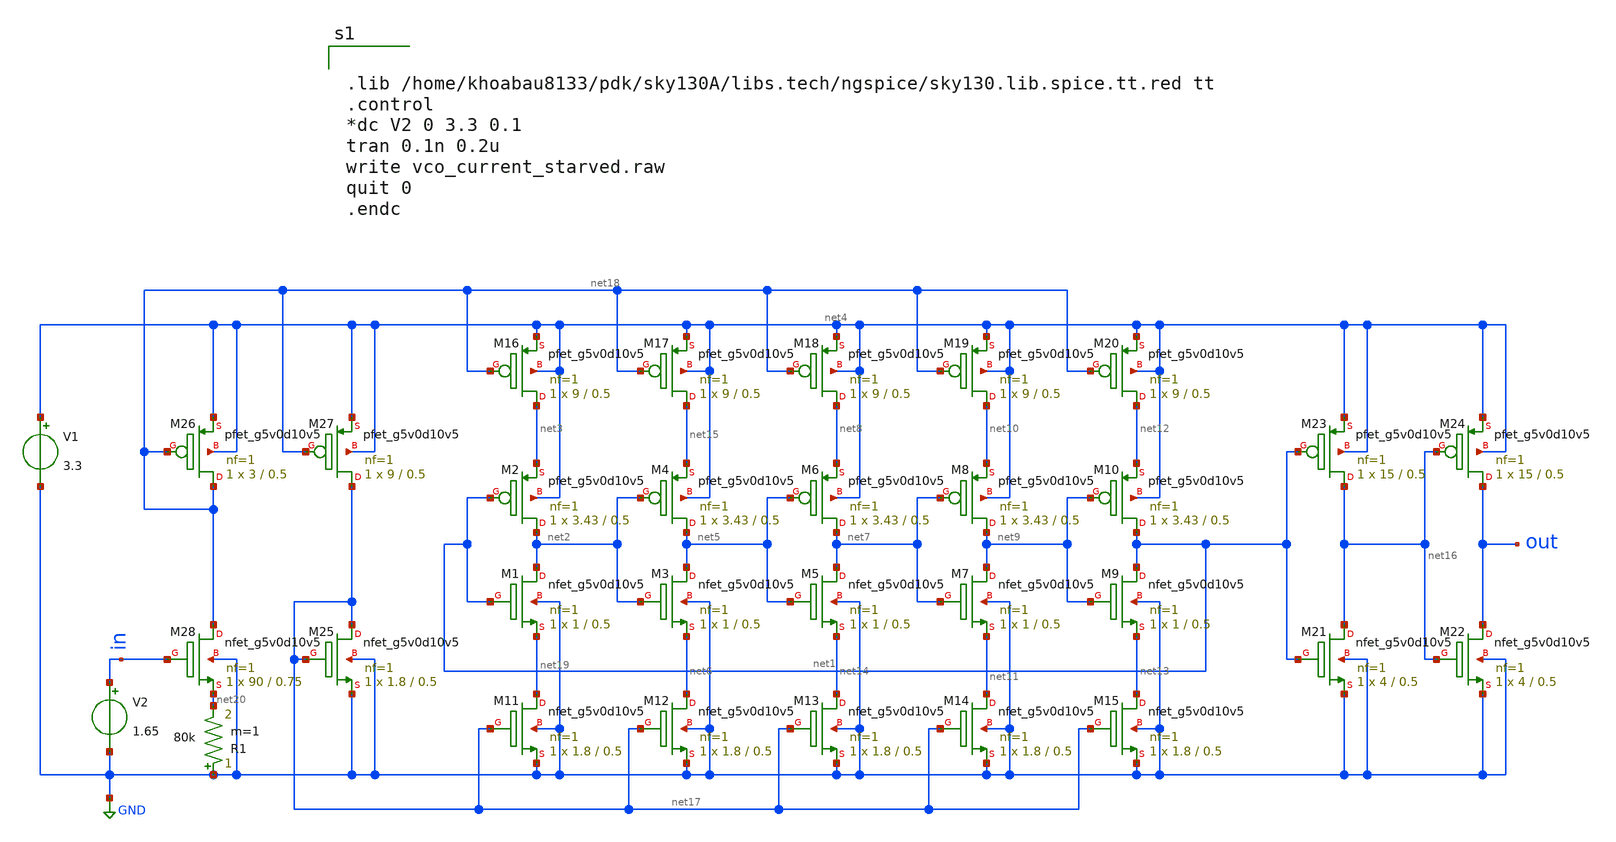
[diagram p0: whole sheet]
** sch_path: Voltage-controlled Oscillator/test_VCO_v3.sch
**.subckt test_VCO_v3
V1 net4 GND 3.3
V2 in GND 1.65
R1 GND net20 80k m=1
XM1 net2 net1 net19 GND sky130_fd_pr__nfet_g5v0d10v5 L=0.5 W=1 nf=1 ad='int((nf+1)/2) * W/nf * 0.29'
+ as='int((nf+2)/2) * W/nf * 0.29' pd='2*int((nf+1)/2) * (W/nf + 0.29)' ps='2*int((nf+2)/2) * (W/nf + 0.29)'
+ nrd='0.29 / W' nrs='0.29 / W' sa=0 sb=0 sd=0 mult=1 m=1
XM2 net2 net1 net3 net4 sky130_fd_pr__pfet_g5v0d10v5 L=0.5 W=3.43 nf=1 ad='int((nf+1)/2) * W/nf * 0.29'
+ as='int((nf+2)/2) * W/nf * 0.29' pd='2*int((nf+1)/2) * (W/nf + 0.29)' ps='2*int((nf+2)/2) * (W/nf + 0.29)'
+ nrd='0.29 / W' nrs='0.29 / W' sa=0 sb=0 sd=0 mult=1 m=1
XM3 net5 net2 net6 GND sky130_fd_pr__nfet_g5v0d10v5 L=0.5 W=1 nf=1 ad='int((nf+1)/2) * W/nf * 0.29' as='int((nf+2)/2) * W/nf * 0.29'
+ pd='2*int((nf+1)/2) * (W/nf + 0.29)' ps='2*int((nf+2)/2) * (W/nf + 0.29)' nrd='0.29 / W' nrs='0.29 / W'
+ sa=0 sb=0 sd=0 mult=1 m=1
XM4 net5 net2 net15 net4 sky130_fd_pr__pfet_g5v0d10v5 L=0.5 W=3.43 nf=1 ad='int((nf+1)/2) * W/nf * 0.29'
+ as='int((nf+2)/2) * W/nf * 0.29' pd='2*int((nf+1)/2) * (W/nf + 0.29)' ps='2*int((nf+2)/2) * (W/nf + 0.29)'
+ nrd='0.29 / W' nrs='0.29 / W' sa=0 sb=0 sd=0 mult=1 m=1
XM5 net7 net5 net14 GND sky130_fd_pr__nfet_g5v0d10v5 L=0.5 W=1 nf=1 ad='int((nf+1)/2) * W/nf * 0.29'
+ as='int((nf+2)/2) * W/nf * 0.29' pd='2*int((nf+1)/2) * (W/nf + 0.29)' ps='2*int((nf+2)/2) * (W/nf + 0.29)'
+ nrd='0.29 / W' nrs='0.29 / W' sa=0 sb=0 sd=0 mult=1 m=1
XM6 net7 net5 net8 net4 sky130_fd_pr__pfet_g5v0d10v5 L=0.5 W=3.43 nf=1 ad='int((nf+1)/2) * W/nf * 0.29'
+ as='int((nf+2)/2) * W/nf * 0.29' pd='2*int((nf+1)/2) * (W/nf + 0.29)' ps='2*int((nf+2)/2) * (W/nf + 0.29)'
+ nrd='0.29 / W' nrs='0.29 / W' sa=0 sb=0 sd=0 mult=1 m=1
XM7 net9 net7 net11 GND sky130_fd_pr__nfet_g5v0d10v5 L=0.5 W=1 nf=1 ad='int((nf+1)/2) * W/nf * 0.29'
+ as='int((nf+2)/2) * W/nf * 0.29' pd='2*int((nf+1)/2) * (W/nf + 0.29)' ps='2*int((nf+2)/2) * (W/nf + 0.29)'
+ nrd='0.29 / W' nrs='0.29 / W' sa=0 sb=0 sd=0 mult=1 m=1
XM8 net9 net7 net10 net4 sky130_fd_pr__pfet_g5v0d10v5 L=0.5 W=3.43 nf=1 ad='int((nf+1)/2) * W/nf * 0.29'
+ as='int((nf+2)/2) * W/nf * 0.29' pd='2*int((nf+1)/2) * (W/nf + 0.29)' ps='2*int((nf+2)/2) * (W/nf + 0.29)'
+ nrd='0.29 / W' nrs='0.29 / W' sa=0 sb=0 sd=0 mult=1 m=1
XM9 net1 net9 net13 GND sky130_fd_pr__nfet_g5v0d10v5 L=0.5 W=1 nf=1 ad='int((nf+1)/2) * W/nf * 0.29'
+ as='int((nf+2)/2) * W/nf * 0.29' pd='2*int((nf+1)/2) * (W/nf + 0.29)' ps='2*int((nf+2)/2) * (W/nf + 0.29)'
+ nrd='0.29 / W' nrs='0.29 / W' sa=0 sb=0 sd=0 mult=1 m=1
XM10 net1 net9 net12 net4 sky130_fd_pr__pfet_g5v0d10v5 L=0.5 W=3.43 nf=1 ad='int((nf+1)/2) * W/nf * 0.29'
+ as='int((nf+2)/2) * W/nf * 0.29' pd='2*int((nf+1)/2) * (W/nf + 0.29)' ps='2*int((nf+2)/2) * (W/nf + 0.29)'
+ nrd='0.29 / W' nrs='0.29 / W' sa=0 sb=0 sd=0 mult=1 m=1
XM11 net19 net17 GND GND sky130_fd_pr__nfet_g5v0d10v5 L=0.5 W=1.8 nf=1 ad='int((nf+1)/2) * W/nf * 0.29'
+ as='int((nf+2)/2) * W/nf * 0.29' pd='2*int((nf+1)/2) * (W/nf + 0.29)' ps='2*int((nf+2)/2) * (W/nf + 0.29)'
+ nrd='0.29 / W' nrs='0.29 / W' sa=0 sb=0 sd=0 mult=1 m=1
XM12 net6 net17 GND GND sky130_fd_pr__nfet_g5v0d10v5 L=0.5 W=1.8 nf=1 ad='int((nf+1)/2) * W/nf * 0.29'
+ as='int((nf+2)/2) * W/nf * 0.29' pd='2*int((nf+1)/2) * (W/nf + 0.29)' ps='2*int((nf+2)/2) * (W/nf + 0.29)'
+ nrd='0.29 / W' nrs='0.29 / W' sa=0 sb=0 sd=0 mult=1 m=1
XM13 net14 net17 GND GND sky130_fd_pr__nfet_g5v0d10v5 L=0.5 W=1.8 nf=1 ad='int((nf+1)/2) * W/nf * 0.29'
+ as='int((nf+2)/2) * W/nf * 0.29' pd='2*int((nf+1)/2) * (W/nf + 0.29)' ps='2*int((nf+2)/2) * (W/nf + 0.29)'
+ nrd='0.29 / W' nrs='0.29 / W' sa=0 sb=0 sd=0 mult=1 m=1
XM14 net11 net17 GND GND sky130_fd_pr__nfet_g5v0d10v5 L=0.5 W=1.8 nf=1 ad='int((nf+1)/2) * W/nf * 0.29'
+ as='int((nf+2)/2) * W/nf * 0.29' pd='2*int((nf+1)/2) * (W/nf + 0.29)' ps='2*int((nf+2)/2) * (W/nf + 0.29)'
+ nrd='0.29 / W' nrs='0.29 / W' sa=0 sb=0 sd=0 mult=1 m=1
XM15 net13 net17 GND GND sky130_fd_pr__nfet_g5v0d10v5 L=0.5 W=1.8 nf=1 ad='int((nf+1)/2) * W/nf * 0.29'
+ as='int((nf+2)/2) * W/nf * 0.29' pd='2*int((nf+1)/2) * (W/nf + 0.29)' ps='2*int((nf+2)/2) * (W/nf + 0.29)'
+ nrd='0.29 / W' nrs='0.29 / W' sa=0 sb=0 sd=0 mult=1 m=1
XM16 net3 net18 net4 net4 sky130_fd_pr__pfet_g5v0d10v5 L=0.5 W=9 nf=1 ad='int((nf+1)/2) * W/nf * 0.29'
+ as='int((nf+2)/2) * W/nf * 0.29' pd='2*int((nf+1)/2) * (W/nf + 0.29)' ps='2*int((nf+2)/2) * (W/nf + 0.29)'
+ nrd='0.29 / W' nrs='0.29 / W' sa=0 sb=0 sd=0 mult=1 m=1
XM17 net15 net18 net4 net4 sky130_fd_pr__pfet_g5v0d10v5 L=0.5 W=9 nf=1 ad='int((nf+1)/2) * W/nf * 0.29'
+ as='int((nf+2)/2) * W/nf * 0.29' pd='2*int((nf+1)/2) * (W/nf + 0.29)' ps='2*int((nf+2)/2) * (W/nf + 0.29)'
+ nrd='0.29 / W' nrs='0.29 / W' sa=0 sb=0 sd=0 mult=1 m=1
XM18 net8 net18 net4 net4 sky130_fd_pr__pfet_g5v0d10v5 L=0.5 W=9 nf=1 ad='int((nf+1)/2) * W/nf * 0.29'
+ as='int((nf+2)/2) * W/nf * 0.29' pd='2*int((nf+1)/2) * (W/nf + 0.29)' ps='2*int((nf+2)/2) * (W/nf + 0.29)'
+ nrd='0.29 / W' nrs='0.29 / W' sa=0 sb=0 sd=0 mult=1 m=1
XM19 net10 net18 net4 net4 sky130_fd_pr__pfet_g5v0d10v5 L=0.5 W=9 nf=1 ad='int((nf+1)/2) * W/nf * 0.29'
+ as='int((nf+2)/2) * W/nf * 0.29' pd='2*int((nf+1)/2) * (W/nf + 0.29)' ps='2*int((nf+2)/2) * (W/nf + 0.29)'
+ nrd='0.29 / W' nrs='0.29 / W' sa=0 sb=0 sd=0 mult=1 m=1
XM20 net12 net18 net4 net4 sky130_fd_pr__pfet_g5v0d10v5 L=0.5 W=9 nf=1 ad='int((nf+1)/2) * W/nf * 0.29'
+ as='int((nf+2)/2) * W/nf * 0.29' pd='2*int((nf+1)/2) * (W/nf + 0.29)' ps='2*int((nf+2)/2) * (W/nf + 0.29)'
+ nrd='0.29 / W' nrs='0.29 / W' sa=0 sb=0 sd=0 mult=1 m=1
XM21 net16 net1 GND GND sky130_fd_pr__nfet_g5v0d10v5 L=0.5 W=4 nf=1 ad='int((nf+1)/2) * W/nf * 0.29'
+ as='int((nf+2)/2) * W/nf * 0.29' pd='2*int((nf+1)/2) * (W/nf + 0.29)' ps='2*int((nf+2)/2) * (W/nf + 0.29)'
+ nrd='0.29 / W' nrs='0.29 / W' sa=0 sb=0 sd=0 mult=1 m=1
XM22 out net16 GND GND sky130_fd_pr__nfet_g5v0d10v5 L=0.5 W=4 nf=1 ad='int((nf+1)/2) * W/nf * 0.29' as='int((nf+2)/2) * W/nf * 0.29'
+ pd='2*int((nf+1)/2) * (W/nf + 0.29)' ps='2*int((nf+2)/2) * (W/nf + 0.29)' nrd='0.29 / W' nrs='0.29 / W'
+ sa=0 sb=0 sd=0 mult=1 m=1
XM23 net16 net1 net4 net4 sky130_fd_pr__pfet_g5v0d10v5 L=0.5 W=15 nf=1 ad='int((nf+1)/2) * W/nf * 0.29'
+ as='int((nf+2)/2) * W/nf * 0.29' pd='2*int((nf+1)/2) * (W/nf + 0.29)' ps='2*int((nf+2)/2) * (W/nf + 0.29)'
+ nrd='0.29 / W' nrs='0.29 / W' sa=0 sb=0 sd=0 mult=1 m=1
XM24 out net16 net4 net4 sky130_fd_pr__pfet_g5v0d10v5 L=0.5 W=15 nf=1 ad='int((nf+1)/2) * W/nf * 0.29'
+ as='int((nf+2)/2) * W/nf * 0.29' pd='2*int((nf+1)/2) * (W/nf + 0.29)' ps='2*int((nf+2)/2) * (W/nf + 0.29)'
+ nrd='0.29 / W' nrs='0.29 / W' sa=0 sb=0 sd=0 mult=1 m=1
XM25 net17 net17 GND GND sky130_fd_pr__nfet_g5v0d10v5 L=0.5 W=1.8 nf=1 ad='int((nf+1)/2) * W/nf * 0.29'
+ as='int((nf+2)/2) * W/nf * 0.29' pd='2*int((nf+1)/2) * (W/nf + 0.29)' ps='2*int((nf+2)/2) * (W/nf + 0.29)'
+ nrd='0.29 / W' nrs='0.29 / W' sa=0 sb=0 sd=0 mult=1 m=1
XM26 net18 net18 net4 net4 sky130_fd_pr__pfet_g5v0d10v5 L=0.5 W=3 nf=1 ad='int((nf+1)/2) * W/nf * 0.29'
+ as='int((nf+2)/2) * W/nf * 0.29' pd='2*int((nf+1)/2) * (W/nf + 0.29)' ps='2*int((nf+2)/2) * (W/nf + 0.29)'
+ nrd='0.29 / W' nrs='0.29 / W' sa=0 sb=0 sd=0 mult=1 m=1
XM27 net17 net18 net4 net4 sky130_fd_pr__pfet_g5v0d10v5 L=0.5 W=9 nf=1 ad='int((nf+1)/2) * W/nf * 0.29'
+ as='int((nf+2)/2) * W/nf * 0.29' pd='2*int((nf+1)/2) * (W/nf + 0.29)' ps='2*int((nf+2)/2) * (W/nf + 0.29)'
+ nrd='0.29 / W' nrs='0.29 / W' sa=0 sb=0 sd=0 mult=1 m=1
XM28 net18 in net20 GND sky130_fd_pr__nfet_g5v0d10v5 L=0.75 W=90 nf=1 ad='int((nf+1)/2) * W/nf * 0.29'
+ as='int((nf+2)/2) * W/nf * 0.29' pd='2*int((nf+1)/2) * (W/nf + 0.29)' ps='2*int((nf+2)/2) * (W/nf + 0.29)'
+ nrd='0.29 / W' nrs='0.29 / W' sa=0 sb=0 sd=0 mult=1 m=1
**** begin user architecture code


.lib /home/khoabau8133/pdk/sky130A/libs.tech/ngspice/sky130.lib.spice.tt.red tt
.control
*dc V2 0 3.3 0.1
tran 0.1n 0.2u
write vco_current_starved.raw
quit 0
.endc


**** end user architecture code
**.ends
.GLOBAL GND
.end
